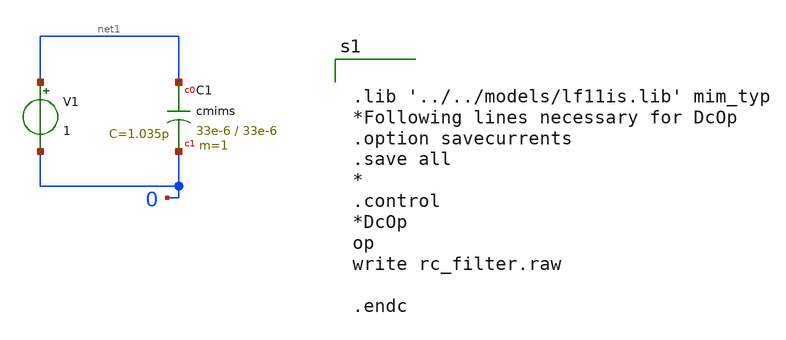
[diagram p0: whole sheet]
** sch_path: test_cmimsLF.sch
**.subckt test_cmimsLF
XC1 net1 0 cmims w=33e-6 l=33e-6 m=1
V1 net1 0 1
**** begin user architecture code


.lib '../../models/lf11is.lib' mim_typ
*Following lines necessary for DcOp
.option savecurrents
.save all
*
.control
*DcOp
op
write rc_filter.raw

.endc


**** end user architecture code
**.ends
.end
